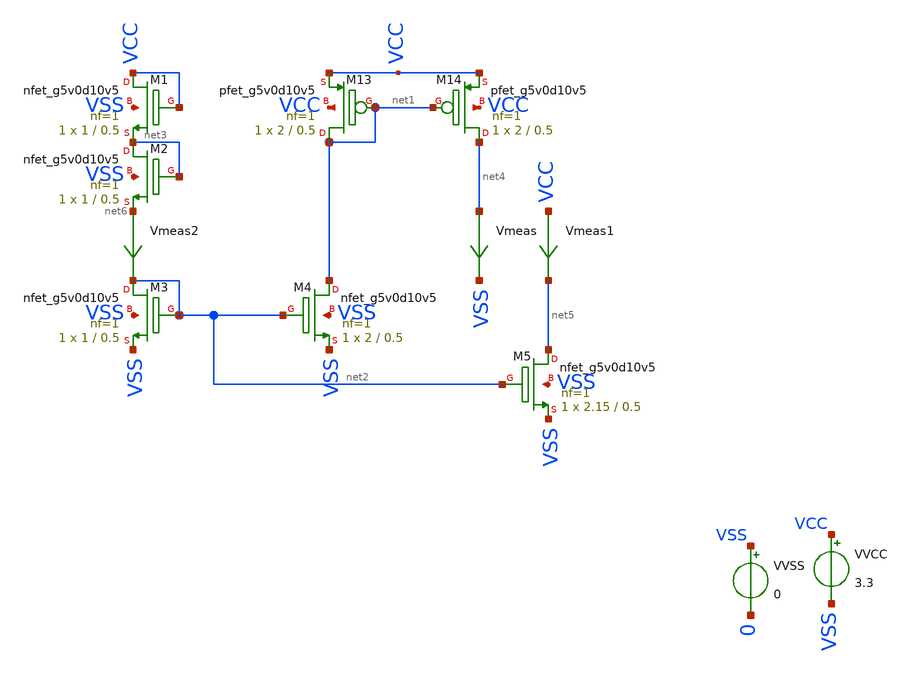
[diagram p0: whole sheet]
** sch_path: Comparator/schematic/folded_cascode/older/cs.sch
.lib $::SKYWATER_MODELS/sky130.lib.spice.tt.red tt
.include $::SKYWATER_STDCELLS/sky130_fd_sc_hd.spice

**.subckt cs
VVSS VSS 0 0
VVCC VCC VSS 3.3
XM13 net1 net1 VCC VCC sky130_fd_pr__pfet_g5v0d10v5 L=0.5 W=2 nf=1 ad='int((nf+1)/2) * W/nf * 0.29' as='int((nf+2)/2) * W/nf * 0.29'
+ pd='2*int((nf+1)/2) * (W/nf + 0.29)' ps='2*int((nf+2)/2) * (W/nf + 0.29)' nrd='0.29 / W' nrs='0.29 / W'
+ sa=0 sb=0 sd=0 mult=1 m=1
XM14 net4 net1 VCC VCC sky130_fd_pr__pfet_g5v0d10v5 L=0.5 W=2 nf=1 ad='int((nf+1)/2) * W/nf * 0.29' as='int((nf+2)/2) * W/nf * 0.29'
+ pd='2*int((nf+1)/2) * (W/nf + 0.29)' ps='2*int((nf+2)/2) * (W/nf + 0.29)' nrd='0.29 / W' nrs='0.29 / W'
+ sa=0 sb=0 sd=0 mult=1 m=1
Vmeas net4 VSS 0
.save i(vmeas)
XM3 net2 net2 VSS VSS sky130_fd_pr__nfet_g5v0d10v5 L=0.5 W=1 nf=1 ad='int((nf+1)/2) * W/nf * 0.29' as='int((nf+2)/2) * W/nf * 0.29'
+ pd='2*int((nf+1)/2) * (W/nf + 0.29)' ps='2*int((nf+2)/2) * (W/nf + 0.29)' nrd='0.29 / W' nrs='0.29 / W'
+ sa=0 sb=0 sd=0 mult=1 m=1
XM4 net1 net2 VSS VSS sky130_fd_pr__nfet_g5v0d10v5 L=0.5 W=2 nf=1 ad='int((nf+1)/2) * W/nf * 0.29' as='int((nf+2)/2) * W/nf * 0.29'
+ pd='2*int((nf+1)/2) * (W/nf + 0.29)' ps='2*int((nf+2)/2) * (W/nf + 0.29)' nrd='0.29 / W' nrs='0.29 / W'
+ sa=0 sb=0 sd=0 mult=1 m=1
Vmeas2 net6 net2 0
.save i(vmeas2)
XM1 VCC VCC net3 VSS sky130_fd_pr__nfet_g5v0d10v5 L=0.5 W=1 nf=1 ad='int((nf+1)/2) * W/nf * 0.29' as='int((nf+2)/2) * W/nf * 0.29'
+ pd='2*int((nf+1)/2) * (W/nf + 0.29)' ps='2*int((nf+2)/2) * (W/nf + 0.29)' nrd='0.29 / W' nrs='0.29 / W'
+ sa=0 sb=0 sd=0 mult=1 m=1
XM2 net3 net3 net6 VSS sky130_fd_pr__nfet_g5v0d10v5 L=0.5 W=1 nf=1 ad='int((nf+1)/2) * W/nf * 0.29' as='int((nf+2)/2) * W/nf * 0.29'
+ pd='2*int((nf+1)/2) * (W/nf + 0.29)' ps='2*int((nf+2)/2) * (W/nf + 0.29)' nrd='0.29 / W' nrs='0.29 / W'
+ sa=0 sb=0 sd=0 mult=1 m=1
XM5 net5 net2 VSS VSS sky130_fd_pr__nfet_g5v0d10v5 L=0.5 W=2.15 nf=1 ad='int((nf+1)/2) * W/nf * 0.29'
+ as='int((nf+2)/2) * W/nf * 0.29' pd='2*int((nf+1)/2) * (W/nf + 0.29)' ps='2*int((nf+2)/2) * (W/nf + 0.29)'
+ nrd='0.29 / W' nrs='0.29 / W' sa=0 sb=0 sd=0 mult=1 m=1
Vmeas1 VCC net5 0
.save i(vmeas1)
**** begin user architecture code


*.option savecurrents
.tran 1n 50n
*.dc VVCC 0 3.3 0.1
**** interactive sim
.control
set color0=white
run

write cs.raw
*quit
.endc


**** end user architecture code
**.ends
.end
